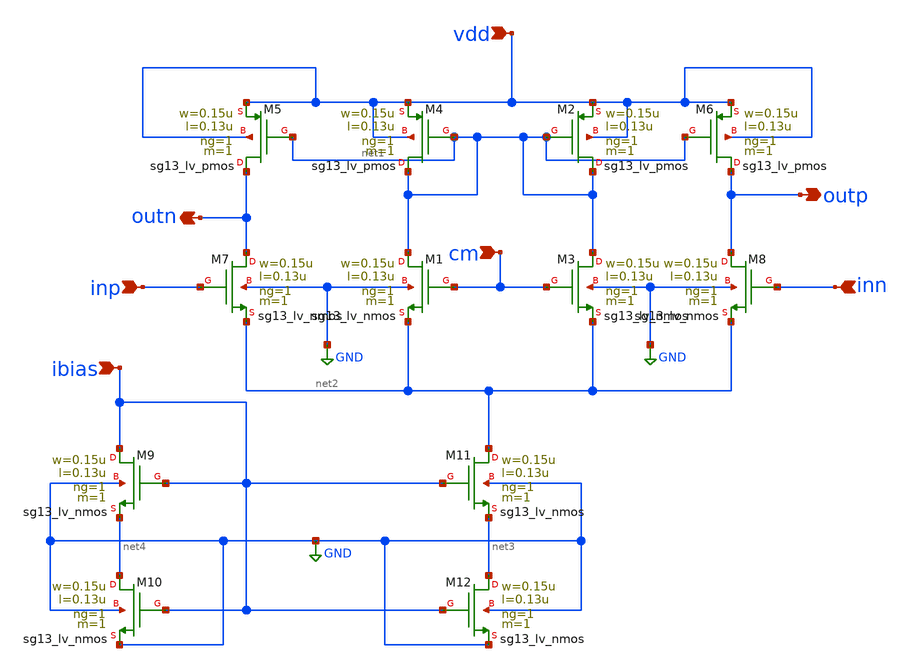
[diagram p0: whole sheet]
** sch_path: 3_Real_Cir/10_Real_Cir/ota_gm_100u.sch
**.subckt ota_gm_100u inp vdd inn outp cm ibias outn
*.ipin inp
*.ipin vdd
*.ipin inn
*.opin outp
*.ipin cm
*.ipin ibias
*.opin outn
XM1 net1 cm net2 GND sg13_lv_nmos w=0.15u l=0.13u ng=1 m=1 mm_ok=1
XM2 net1 net1 vdd vdd sg13_lv_pmos w=0.15u l=0.13u ng=1 m=1 mm_ok=1
XM3 net1 cm net2 GND sg13_lv_nmos w=0.15u l=0.13u ng=1 m=1 mm_ok=1
XM4 net1 net1 vdd vdd sg13_lv_pmos w=0.15u l=0.13u ng=1 m=1 mm_ok=1
XM5 outn net1 vdd vdd sg13_lv_pmos w=0.15u l=0.13u ng=1 m=1 mm_ok=1
XM6 outp net1 vdd vdd sg13_lv_pmos w=0.15u l=0.13u ng=1 m=1 mm_ok=1
XM7 outn inp net2 GND sg13_lv_nmos w=0.15u l=0.13u ng=1 m=1 mm_ok=1
XM8 outp inn net2 GND sg13_lv_nmos w=0.15u l=0.13u ng=1 m=1 mm_ok=1
XM9 ibias ibias net4 GND sg13_lv_nmos w=0.15u l=0.13u ng=1 m=1 mm_ok=1
XM11 net2 ibias net3 GND sg13_lv_nmos w=0.15u l=0.13u ng=1 m=1 mm_ok=1
XM10 net4 ibias GND GND sg13_lv_nmos w=0.15u l=0.13u ng=1 m=1 mm_ok=1
XM12 net3 ibias GND GND sg13_lv_nmos w=0.15u l=0.13u ng=1 m=1 mm_ok=1
**.ends
.GLOBAL GND
.end
